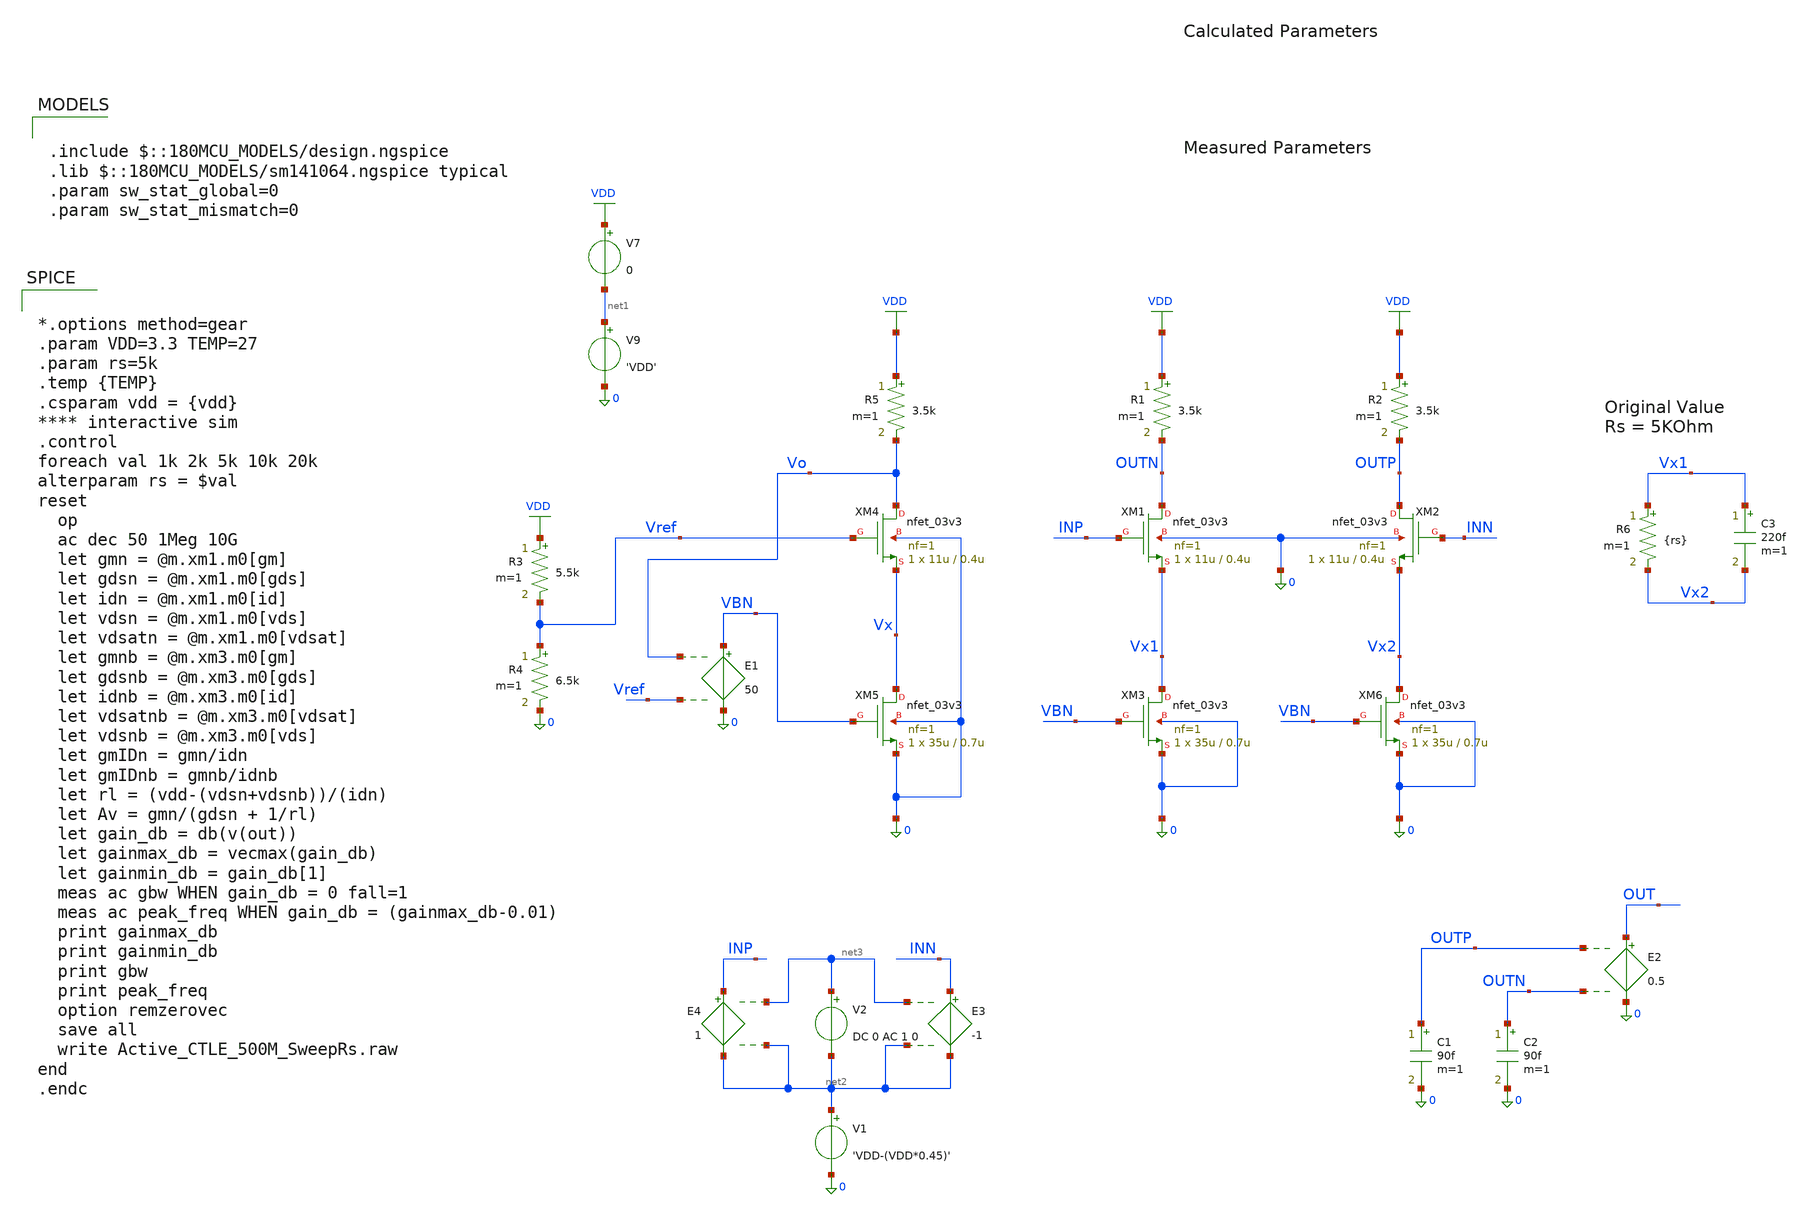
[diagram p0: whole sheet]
** sch_path: Xschem/gf180mcuD/gmID_Designs/Active_CTLE_500M_SweepRs.sch
**.subckt Active_CTLE_500M_SweepRs
XM1 OUTN INP Vx1 0 nfet_03v3 L=0.4u W=11u nf=1 ad='int((nf+1)/2) * W/nf * 0.18u' as='int((nf+2)/2) * W/nf * 0.18u'
+ pd='2*int((nf+1)/2) * (W/nf + 0.18u)' ps='2*int((nf+2)/2) * (W/nf + 0.18u)' nrd='0.18u / W' nrs='0.18u / W'
+ sa=0 sb=0 sd=0 m=1
E1 VBN 0 Vo Vref 50
V9 net1 0 'VDD'
V7 VDD net1 0
C2 OUTN 0 90f m=1
XM2 OUTP INN Vx2 0 nfet_03v3 L=0.4u W=11u nf=1 ad='int((nf+1)/2) * W/nf * 0.18u' as='int((nf+2)/2) * W/nf * 0.18u'
+ pd='2*int((nf+1)/2) * (W/nf + 0.18u)' ps='2*int((nf+2)/2) * (W/nf + 0.18u)' nrd='0.18u / W' nrs='0.18u / W'
+ sa=0 sb=0 sd=0 m=1
R1 VDD OUTN 3.5k m=1
R2 VDD OUTP 3.5k m=1
XM3 Vx1 VBN 0 0 nfet_03v3 L=0.7u W=35u nf=1 ad='int((nf+1)/2) * W/nf * 0.18u' as='int((nf+2)/2) * W/nf * 0.18u'
+ pd='2*int((nf+1)/2) * (W/nf + 0.18u)' ps='2*int((nf+2)/2) * (W/nf + 0.18u)' nrd='0.18u / W' nrs='0.18u / W'
+ sa=0 sb=0 sd=0 m=1
E2 OUT 0 OUTP OUTN 0.5
C1 OUTP 0 90f m=1
R3 VDD Vref 5.5k m=1
R4 Vref 0 6.5k m=1
XM4 Vo Vref Vx 0 nfet_03v3 L=0.4u W=11u nf=1 ad='int((nf+1)/2) * W/nf * 0.18u' as='int((nf+2)/2) * W/nf * 0.18u'
+ pd='2*int((nf+1)/2) * (W/nf + 0.18u)' ps='2*int((nf+2)/2) * (W/nf + 0.18u)' nrd='0.18u / W' nrs='0.18u / W'
+ sa=0 sb=0 sd=0 m=1
XM5 Vx VBN 0 0 nfet_03v3 L=0.7u W=35u nf=1 ad='int((nf+1)/2) * W/nf * 0.18u' as='int((nf+2)/2) * W/nf * 0.18u'
+ pd='2*int((nf+1)/2) * (W/nf + 0.18u)' ps='2*int((nf+2)/2) * (W/nf + 0.18u)' nrd='0.18u / W' nrs='0.18u / W'
+ sa=0 sb=0 sd=0 m=1
R5 VDD Vo 3.5k m=1
E3 INN net2 net3 net2 -1
V1 net2 0 'VDD-(VDD*0.45)'
V2 net3 net2 DC 0 AC 1 0
E4 INP net2 net3 net2 1
XM6 Vx2 VBN 0 0 nfet_03v3 L=0.7u W=35u nf=1 ad='int((nf+1)/2) * W/nf * 0.18u' as='int((nf+2)/2) * W/nf * 0.18u'
+ pd='2*int((nf+1)/2) * (W/nf + 0.18u)' ps='2*int((nf+2)/2) * (W/nf + 0.18u)' nrd='0.18u / W' nrs='0.18u / W'
+ sa=0 sb=0 sd=0 m=1
R6 Vx1 Vx2 {rs} m=1
C3 Vx1 Vx2 220f m=1
**** begin user architecture code

.include $::180MCU_MODELS/design.ngspice
.lib $::180MCU_MODELS/sm141064.ngspice typical
.param sw_stat_global=0
.param sw_stat_mismatch=0



*.options method=gear
.param VDD=3.3 TEMP=27
.param rs=5k
.temp {TEMP}
.csparam vdd = {vdd}
**** interactive sim
.control
foreach val 1k 2k 5k 10k 20k
alterparam rs = $val
reset
  op
  ac dec 50 1Meg 10G
  let gmn = @m.xm1.m0[gm]
  let gdsn = @m.xm1.m0[gds]
  let idn = @m.xm1.m0[id]
  let vdsn = @m.xm1.m0[vds]
  let vdsatn = @m.xm1.m0[vdsat]
  let gmnb = @m.xm3.m0[gm]
  let gdsnb = @m.xm3.m0[gds]
  let idnb = @m.xm3.m0[id]
  let vdsatnb = @m.xm3.m0[vdsat]
  let vdsnb = @m.xm3.m0[vds]
  let gmIDn = gmn/idn
  let gmIDnb = gmnb/idnb
  let rl = (vdd-(vdsn+vdsnb))/(idn)
  let Av = gmn/(gdsn + 1/rl)
  let gain_db = db(v(out))
  let gainmax_db = vecmax(gain_db)
  let gainmin_db = gain_db[1]
  meas ac gbw WHEN gain_db = 0 fall=1
  meas ac peak_freq WHEN gain_db = (gainmax_db-0.01)
  print gainmax_db
  print gainmin_db
  print gbw
  print peak_freq
  option remzerovec
  save all
  write Active_CTLE_500M_SweepRs.raw
end
.endc


**** end user architecture code
**.ends
.GLOBAL VDD
.end
